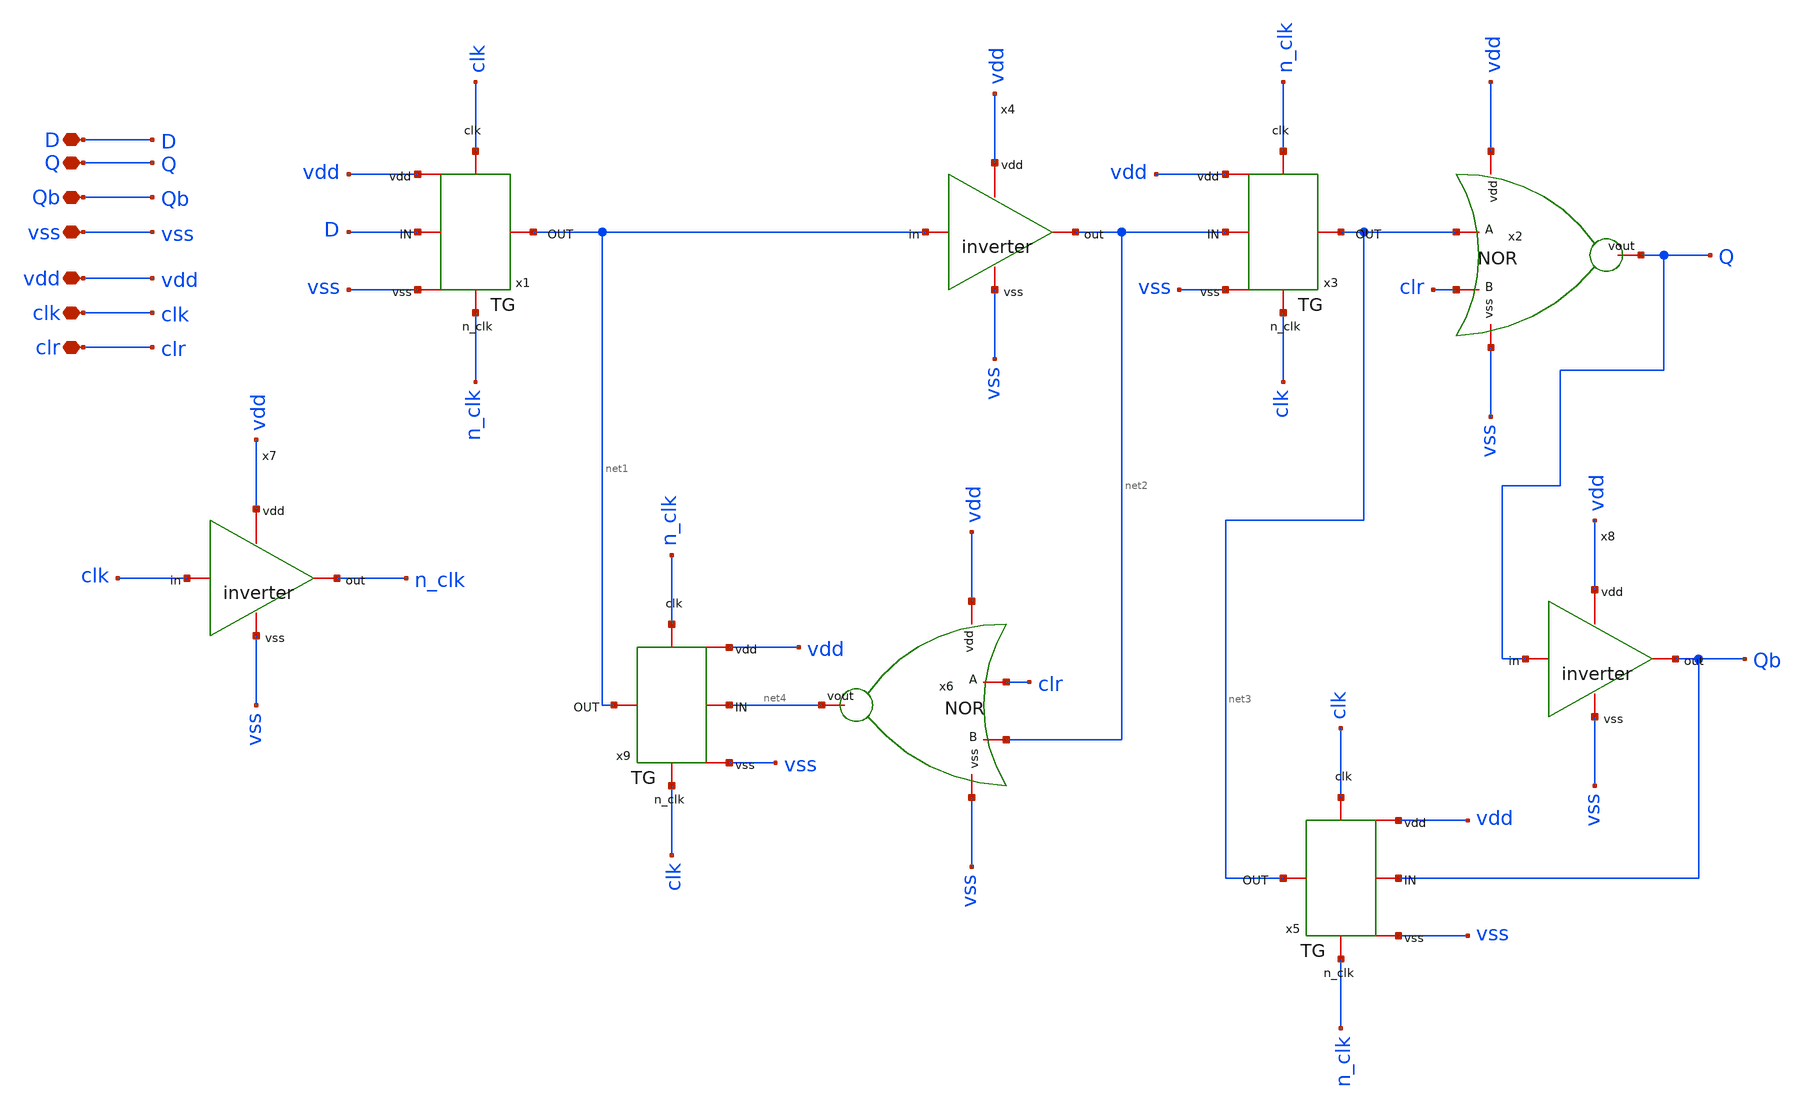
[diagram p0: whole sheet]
** sch_path: sch/FF.sch
**.subckt FF clk clr vdd vss D Q Qb
*.iopin clk
*.iopin clr
*.iopin vdd
*.iopin vss
*.iopin D
*.iopin Q
*.iopin Qb
x1 clk vdd vss D net1 n_clk TG
x3 n_clk vdd vss net2 net3 clk TG
x5 clk vdd vss Qb net3 n_clk TG
x9 n_clk vdd vss net4 net1 clk TG
x2 vss vdd net3 clr Q NOR
x6 vss vdd clr net2 net4 NOR
x4 vdd net1 net2 vss inverter
x7 vdd clk n_clk vss inverter
x8 vdd Q Qb vss inverter
**.ends

* expanding   symbol:  /foss/designs/sch/TG.sym # of pins=6
** sym_path: sch/TG.sym
** sch_path: sch/TG.sch
.subckt TG clk vdd vss IN OUT n_clk
*.iopin OUT
*.iopin IN
*.iopin clk
*.iopin n_clk
*.iopin vdd
*.iopin vss
XM1 OUT clk IN vss sky130_fd_pr__nfet_01v8 L=0.15 W=0.75 nf=1 ad='int((nf+1)/2) * W/nf * 0.29' as='int((nf+2)/2) * W/nf * 0.29'
+ pd='2*int((nf+1)/2) * (W/nf + 0.29)' ps='2*int((nf+2)/2) * (W/nf + 0.29)' nrd='0.29 / W' nrs='0.29 / W'
+ sa=0 sb=0 sd=0 mult=1 m=1
XM2 OUT n_clk IN vdd sky130_fd_pr__pfet_01v8 L=0.15 W=1.5 nf=1 ad='int((nf+1)/2) * W/nf * 0.29' as='int((nf+2)/2) * W/nf * 0.29'
+ pd='2*int((nf+1)/2) * (W/nf + 0.29)' ps='2*int((nf+2)/2) * (W/nf + 0.29)' nrd='0.29 / W' nrs='0.29 / W'
+ sa=0 sb=0 sd=0 mult=1 m=1
.ends


* expanding   symbol:  /foss/designs/sch/NOR.sym # of pins=5
** sym_path: sch/NOR.sym
** sch_path: sch/NOR.sch
.subckt NOR vss vdd A B vout
*.iopin A
*.iopin vdd
*.iopin vss
*.iopin vout
*.iopin B
XM8 vout A vss vss sky130_fd_pr__nfet_01v8 L=0.15 W=0.75 nf=1 ad='int((1 + 1)/2) * 0.75 / 1 * 0.29' as='int((1 + 2)/2) * 0.75 / 1 * 0.29'
+ pd='2*int((1 + 1)/2) * (0.75 / 1 + 0.29)' ps='2*int((1 + 2)/2) * (0.75 / 1 + 0.29)' nrd='0.29 / 0.75 '
+ nrs='0.29 / 0.75 ' sa=0 sb=0 sd=0 mult=1 m=1
XM9 vout B vss vss sky130_fd_pr__nfet_01v8 L=0.15 W=0.75 nf=1 ad='int((1 + 1)/2) * 0.75 / 1 * 0.29' as='int((1 + 2)/2) * 0.75 / 1 * 0.29'
+ pd='2*int((1 + 1)/2) * (0.75 / 1 + 0.29)' ps='2*int((1 + 2)/2) * (0.75 / 1 + 0.29)' nrd='0.29 / 0.75 '
+ nrs='0.29 / 0.75 ' sa=0 sb=0 sd=0 mult=1 m=1
XM7 vout A net1 vdd sky130_fd_pr__pfet_01v8 L=0.15 W=3 nf=1 ad='int((nf+1)/2) * W/nf * 0.29' as='int((nf+2)/2) * W/nf * 0.29'
+ pd='2*int((nf+1)/2) * (W/nf + 0.29)' ps='2*int((nf+2)/2) * (W/nf + 0.29)' nrd='0.29 / W' nrs='0.29 / W'
+ sa=0 sb=0 sd=0 mult=1 m=1
XM6 net1 B vdd vdd sky130_fd_pr__pfet_01v8 L=0.15 W=3 nf=1 ad='int((nf+1)/2) * W/nf * 0.29' as='int((nf+2)/2) * W/nf * 0.29'
+ pd='2*int((nf+1)/2) * (W/nf + 0.29)' ps='2*int((nf+2)/2) * (W/nf + 0.29)' nrd='0.29 / W' nrs='0.29 / W'
+ sa=0 sb=0 sd=0 mult=1 m=1
.ends


* expanding   symbol:  /foss/designs/sch/inverter.sym # of pins=4
** sym_path: sch/inverter.sym
** sch_path: sch/inverter.sch
.subckt inverter vdd in out vss
*.iopin out
*.iopin vdd
*.iopin vss
*.iopin in
XM1 out in vss vss sky130_fd_pr__nfet_01v8 L=0.15 W=0.45 nf=1 ad='int((nf+1)/2) * W/nf * 0.29' as='int((nf+2)/2) * W/nf * 0.29'
+ pd='2*int((nf+1)/2) * (W/nf + 0.29)' ps='2*int((nf+2)/2) * (W/nf + 0.29)' nrd='0.29 / W' nrs='0.29 / W'
+ sa=0 sb=0 sd=0 mult=1 m=1
XM2 out in vdd vdd sky130_fd_pr__pfet_01v8 L=0.15 W=0.45 nf=1 ad='int((nf+1)/2) * W/nf * 0.29' as='int((nf+2)/2) * W/nf * 0.29'
+ pd='2*int((nf+1)/2) * (W/nf + 0.29)' ps='2*int((nf+2)/2) * (W/nf + 0.29)' nrd='0.29 / W' nrs='0.29 / W'
+ sa=0 sb=0 sd=0 mult=1 m=1
.ends

.end
